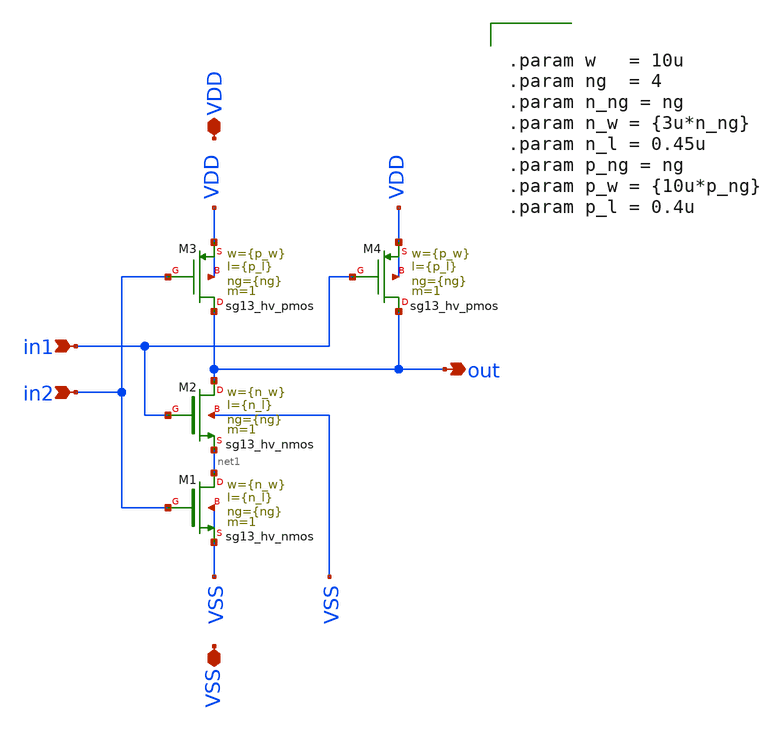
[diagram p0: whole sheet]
** sch_path: macros/heichips26_vcr/macros/switched_capacitor/schematic/xschem/hv_nand.sch
**.subckt hv_nand in1 VDD VSS out in2
*.ipin in1
*.iopin VDD
*.iopin VSS
*.opin out
*.ipin in2
XM2 out in1 net1 VSS sg13_hv_nmos w={n_w} l={n_l} ng={ng} m=1 mm_ok=1
XM3 out in2 VDD VDD sg13_hv_pmos w={p_w} l={p_l} ng={ng} m=1 mm_ok=1
XM1 net1 in2 VSS VSS sg13_hv_nmos w={n_w} l={n_l} ng={ng} m=1 mm_ok=1
XM4 out in1 VDD VDD sg13_hv_pmos w={p_w} l={p_l} ng={ng} m=1 mm_ok=1
**** begin user architecture code


.param w   = 10u
.param ng  = 4
.param n_ng = ng
.param n_w = {3u*n_ng}
.param n_l = 0.45u
.param p_ng = ng
.param p_w = {10u*p_ng}
.param p_l = 0.4u


**** end user architecture code
**.ends
.end
